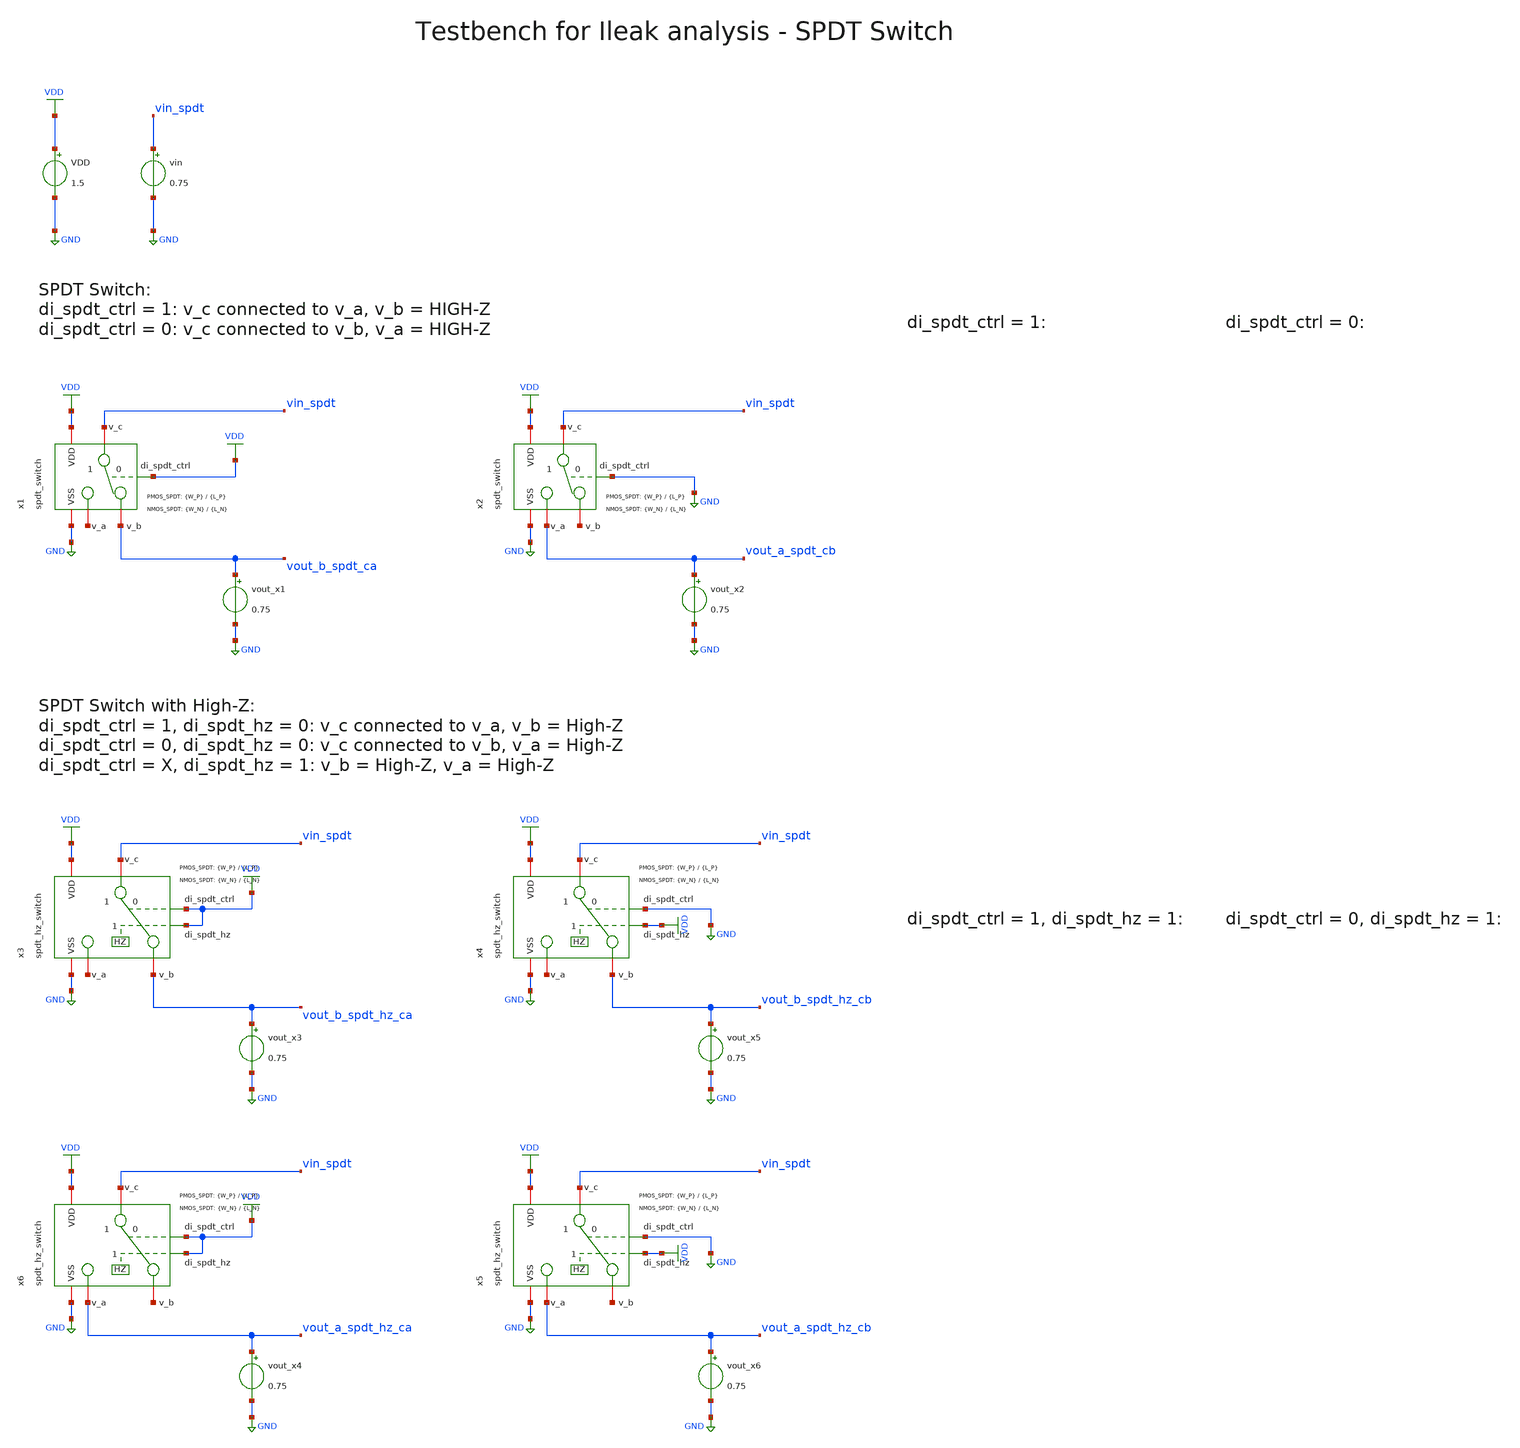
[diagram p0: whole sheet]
** sch_path: SG13G2_ATBS-ADC-main/xschem/spdt_switch/testbenches/spdt_switch_tb_dc_Ileak.sch
**.subckt spdt_switch_tb_dc_Ileak
vout_x1 vout_b_spdt_ca GND 0.75
vout_x2 vout_a_spdt_cb GND 0.75
VDD VDD GND 1.5
vin vin_spdt GND 0.75
x1 VDD VDD GND vin_spdt vout_b_spdt_ca net1 spdt_switch W_P_TG={W_P} L_P_TG={L_P} W_N_TG={W_N} L_N_TG={L_N}
x2 VDD GND GND vin_spdt net2 vout_a_spdt_cb spdt_switch W_P_TG={W_P} L_P_TG={L_P} W_N_TG={W_N} L_N_TG={L_N}
x4 VDD GND GND vin_spdt vout_b_spdt_hz_cb net3 VDD spdt_hz_switch W_P_TG={W_P} L_P_TG={L_P} W_N_TG={W_N}
+ L_N_TG={L_N}
vout_x3 vout_b_spdt_hz_ca GND 0.75
x3 VDD VDD GND vin_spdt vout_b_spdt_hz_ca net4 VDD spdt_hz_switch W_P_TG={W_P} L_P_TG={L_P} W_N_TG={W_N}
+ L_N_TG={L_N}
vout_x5 vout_b_spdt_hz_cb GND 0.75
vout_x4 vout_a_spdt_hz_ca GND 0.75
x5 VDD GND GND vin_spdt net5 vout_a_spdt_hz_cb VDD spdt_hz_switch W_P_TG={W_P} L_P_TG={L_P} W_N_TG={W_N}
+ L_N_TG={L_N}
x6 VDD VDD GND vin_spdt net6 vout_a_spdt_hz_ca VDD spdt_hz_switch W_P_TG={W_P} L_P_TG={L_P} W_N_TG={W_N}
+ L_N_TG={L_N}
vout_x6 vout_a_spdt_hz_cb GND 0.75
**** begin user architecture code

.lib cornerMOSlv.lib mos_tt
.lib cornerRES.lib res_typ



.param temp=27
.param W_N=1u
.param L_N=0.13u
.param W_P=1u
.param L_P=0.13u
.options savecurrents
.control
save all

* Operating Point Analysis
op
remzerovec
write spdt_switch_tb_dc_Ileak.raw
set appendwrite

* DC Sweep Analysis x1
dc vin 0 1.5 10m vout_x1 0 1.5 0.25
write spdt_switch_tb_dc_Ileak.raw
set appendwrite

*Off-Leakage Current v_c to v_b
let Ileak_cb = I(vout_x1)
plot Ileak_cb

* DC Sweep Analysis x2
dc vin 0 1.5 10m vout_x2 0 1.5 0.25
write spdt_switch_tb_dc_Ileak.raw

*Off-Leakage Current v_c to v_a
let Ileak_ca = I(vout_x2)
plot Ileak_ca

* DC Sweep Analysis x3
dc vin 0 1.5 10m vout_x3 0 1.5 0.25
write spdt_switch_tb_dc_Ileak.raw

*Off-Leakage Current v_c to v_b in High-Z
let Ileak_cb_hz = I(vout_x3)
plot Ileak_cb_hz

* DC Sweep Analysis x4
dc vin 0 1.5 10m vout_x4 0 1.5 0.25
write spdt_switch_tb_dc_Ileak.raw

*Off-Leakage Current v_c to v_a in High-Z
let Ileak_ca_hz = I(vout_x4)
plot Ileak_ca_hz

* DC Sweep Analysis x5
dc vin 0 1.5 10m vout_x5 0 1.5 0.25
write spdt_switch_tb_dc_Ileak.raw

*Off-Leakage Current v_c to v_b in High-Z
let Ileak_cb_hz = I(vout_x5)
plot Ileak_cb_hz

* DC Sweep Analysis x6
dc vin 0 1.5 10m vout_x6 0 1.5 0.25
write spdt_switch_tb_dc_Ileak.raw

*Off-Leakage Current v_c to v_a in High-Z
let Ileak_ca_hz = I(vout_x6)
plot Ileak_ca_hz

*quit
.endc

**** end user architecture code
**.ends

* expanding   symbol:  spdt_switch/spdt_switch.sym # of pins=6
** sym_path: SG13G2_ATBS-ADC-main/xschem/spdt_switch/spdt_switch.sym
** sch_path: SG13G2_ATBS-ADC-main/xschem/spdt_switch/spdt_switch.sch
.subckt spdt_switch VDD di_spdt_ctrl VSS v_c v_b v_a  W_P_TG=3.0u L_P_TG=0.13u W_N_TG=1.0u
+ L_N_TG=0.13u
*.iopin v_a
*.iopin v_b
*.iopin v_c
*.iopin VDD
*.iopin VSS
*.ipin di_spdt_ctrl
x1 VDD di_spdt_ctrl VSS v_c v_a di_spdt_ctrl_n transmission_gate_lv_wo_dummy W_P=W_P_TG L_P=L_P_TG
+ W_N=W_N_TG L_N=L_N_TG
x2 VDD di_spdt_ctrl_n VSS v_b v_c di_spdt_ctrl transmission_gate_lv_wo_dummy W_P=W_P_TG L_P=L_P_TG
+ W_N=W_N_TG L_N=L_N_TG
x8 VDD di_spdt_ctrl di_spdt_ctrl_n VSS inverter_lv W_P=W_P_TG L_P=L_P_TG W_N=W_N_TG L_N=L_N_TG
.ends


* expanding   symbol:  spdt_switch/spdt_hz_switch.sym # of pins=7
** sym_path: SG13G2_ATBS-ADC-main/xschem/spdt_switch/spdt_hz_switch.sym
** sch_path: SG13G2_ATBS-ADC-main/xschem/spdt_switch/spdt_hz_switch.sch
.subckt spdt_hz_switch VDD di_spdt_ctrl VSS v_c v_b v_a di_spdt_hz  W_P_TG=3.0u L_P_TG=0.13u
+ W_N_TG=1.0u L_N_TG=0.13u
*.iopin v_a
*.iopin v_b
*.iopin v_c
*.iopin VDD
*.iopin VSS
*.ipin di_spdt_ctrl
*.ipin di_spdt_hz
x1 VDD di_spdt_ctrl VSS net1 v_a di_spdt_ctrl_n transmission_gate_lv_wo_dummy W_P=W_P_TG L_P=L_P_TG
+ W_N=W_N_TG L_N=L_N_TG
x2 VDD di_spdt_ctrl_n VSS v_b net1 di_spdt_ctrl transmission_gate_lv_wo_dummy W_P=W_P_TG L_P=L_P_TG
+ W_N=W_N_TG L_N=L_N_TG
x8 VDD di_spdt_ctrl di_spdt_ctrl_n VSS inverter_lv W_P=W_P_TG L_P=L_P_TG W_N=W_N_TG L_N=L_N_TG
x3 VDD di_spdt_hz di_spdt_hz_n VSS inverter_lv W_P=W_P_TG L_P=L_P_TG W_N=W_N_TG L_N=L_N_TG
x4 VDD di_spdt_hz_n VSS v_c net1 di_spdt_hz transmission_gate_lv_wo_dummy W_P=W_P_TG L_P=L_P_TG
+ W_N=W_N_TG L_N=L_N_TG
.ends


* expanding   symbol:  transmission_gate/transmission_gate_lv_wo_dummy.sym # of pins=6
** sym_path: SG13G2_ATBS-ADC-main/xschem/transmission_gate/transmission_gate_lv_wo_dummy.sym
** sch_path: SG13G2_ATBS-ADC-main/xschem/transmission_gate/transmission_gate_lv_wo_dummy.sch
.subckt transmission_gate_lv_wo_dummy VDD di_tg_ctrl VSS v_b v_a di_tg_ctrl_n  W_P=1.0u L_P=0.13u
+ W_N=1.0u L_N=0.13u
*.iopin v_a
*.iopin v_b
*.iopin VDD
*.iopin VSS
*.ipin di_tg_ctrl
*.ipin di_tg_ctrl_n
XM1 v_a di_tg_ctrl v_b VSS sg13_lv_nmos w=W_N l=L_N ng=1 m=1 mm_ok=1
XM2 v_a di_tg_ctrl_n v_b VDD sg13_lv_pmos w=W_P l=L_P ng=1 m=1 mm_ok=1
.ends


* expanding   symbol:  inverter/inverter_lv.sym # of pins=4
** sym_path: SG13G2_ATBS-ADC-main/xschem/inverter/inverter_lv.sym
** sch_path: SG13G2_ATBS-ADC-main/xschem/inverter/inverter_lv.sch
.subckt inverter_lv VDD vin vout VSS  W_P=3.0u L_P=0.13u W_N=1.0u L_N=0.13u
*.ipin vin
*.iopin VDD
*.iopin VSS
*.opin vout
XM1 vout vin VDD VDD sg13_lv_pmos w=W_P l=L_P ng=1 m=1 mm_ok=1
XM2 vout vin VSS VSS sg13_lv_nmos w=W_N l=L_N ng=1 m=1 mm_ok=1
.ends

.GLOBAL VDD
.GLOBAL GND
.end
